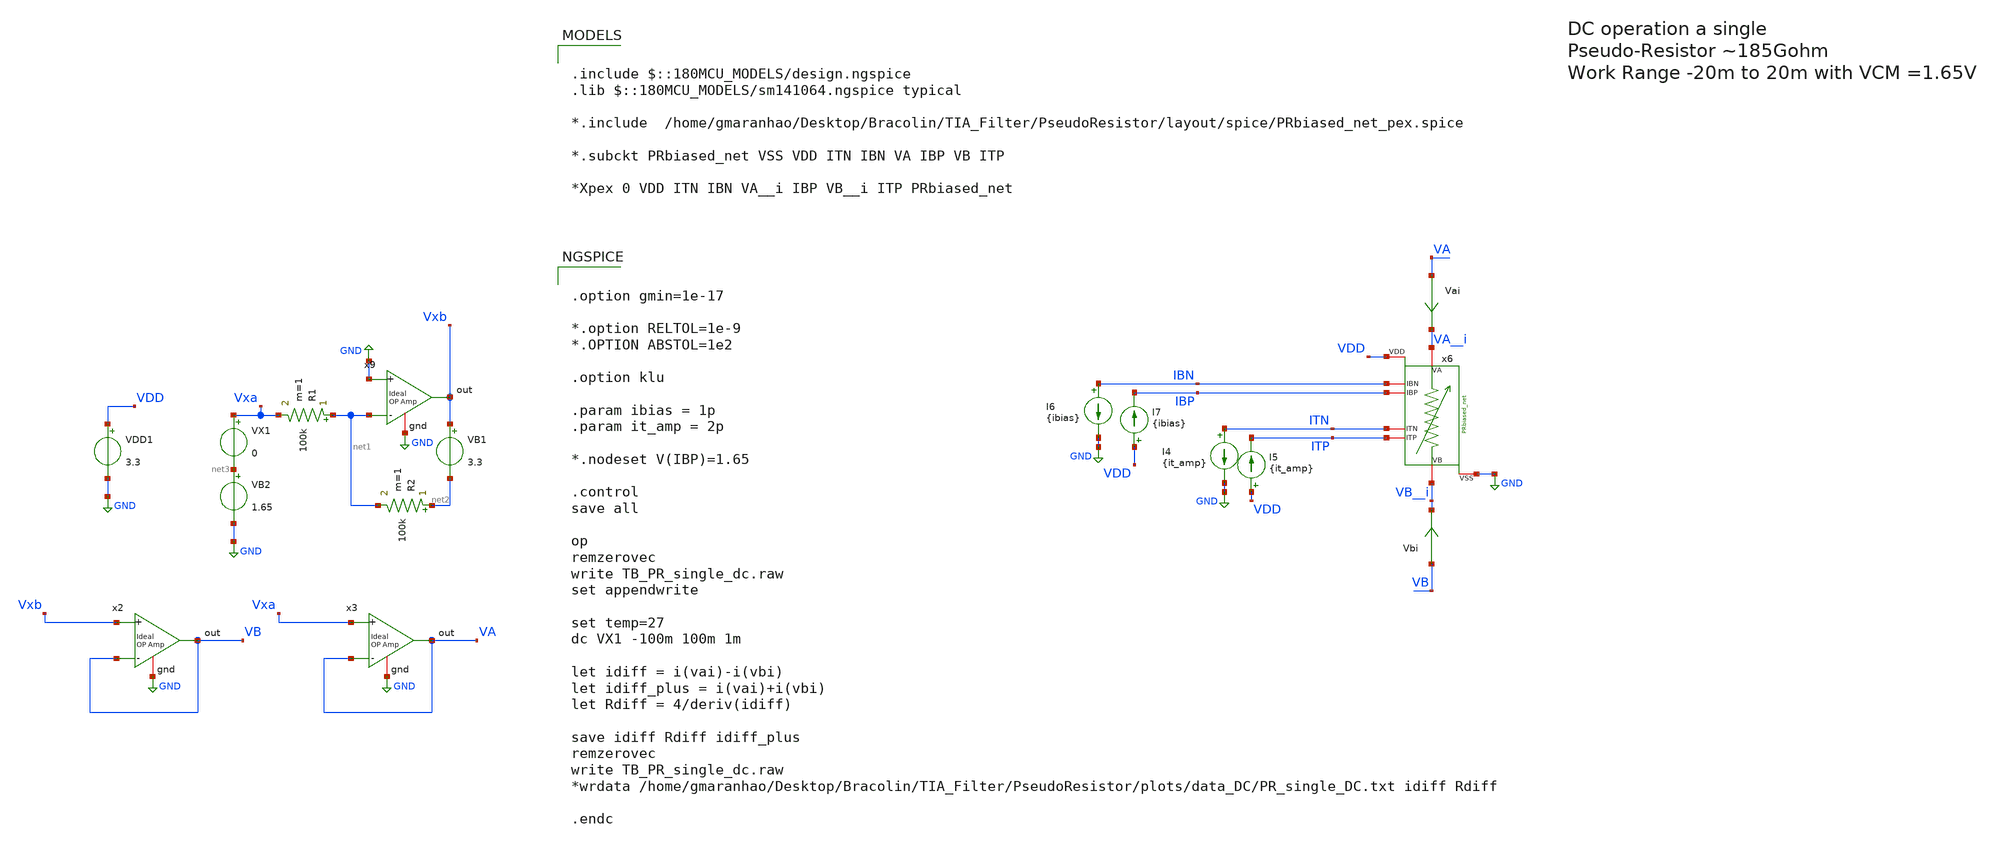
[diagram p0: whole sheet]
** sch_path: TIA_Filter/PseudoResistor/TB_PR_single_dc.sch
**.subckt TB_PR_single_dc
x6 VA__i VB__i IBN IBP ITN ITP VDD GND PRbiased_net
I4 ITN GND {it_amp}
I5 VDD ITP {it_amp}
I6 IBN GND {ibias}
I7 VDD IBP {ibias}
Vai VA VA__i 0
.save i(vai)
Vbi VB VB__i 0
.save i(vbi)
VDD1 VDD GND 3.3
VX1 Vxa net3 0
VB1 Vxb net2 3.3
R1 net1 Vxa 100k m=1
R2 net2 net1 100k m=1
VB2 net3 GND 1.65
x2 VB Vxb VB GND ampOp_ideal
x3 VA Vxa VA GND ampOp_ideal
x9 Vxb GND net1 GND ampOp_ideal
**** begin user architecture code

.include $::180MCU_MODELS/design.ngspice
.lib $::180MCU_MODELS/sm141064.ngspice typical

*.include  /home/gmaranhao/Desktop/Bracolin/TIA_Filter/PseudoResistor/layout/spice/PRbiased_net_pex.spice

*.subckt PRbiased_net VSS VDD ITN IBN VA IBP VB ITP

*Xpex 0 VDD ITN IBN VA__i IBP VB__i ITP PRbiased_net




.option gmin=1e-17

*.option RELTOL=1e-9
*.OPTION ABSTOL=1e2

.option klu

.param ibias = 1p
.param it_amp = 2p

*.nodeset V(IBP)=1.65

.control
save all

op
remzerovec
write TB_PR_single_dc.raw
set appendwrite

set temp=27
dc VX1 -100m 100m 1m

let idiff = i(vai)-i(vbi)
let idiff_plus = i(vai)+i(vbi)
let Rdiff = 4/deriv(idiff)

save idiff Rdiff idiff_plus
remzerovec
write TB_PR_single_dc.raw
*wrdata /home/gmaranhao/Desktop/Bracolin/TIA_Filter/PseudoResistor/plots/data_DC/PR_single_DC.txt
*+ idiff Rdiff

.endc


**** end user architecture code
**.ends
.GLOBAL GND
.end
